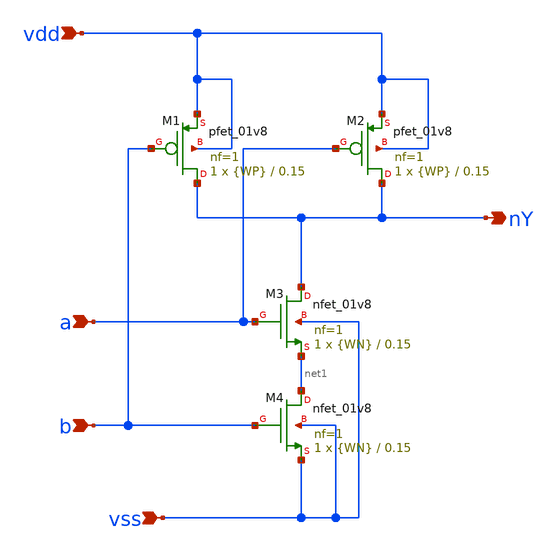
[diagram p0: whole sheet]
** sch_path: eamta2021/sch/nand/schNand.sch
**.subckt schNand vdd vss a b nY
*.ipin vdd
*.ipin vss
*.ipin a
*.ipin b
*.opin nY
XM1 nY b vdd vdd sky130_fd_pr__pfet_01v8 L=0.15 W={WP} nf=1 ad='int((nf+1)/2) * W/nf * 0.29' as='int((nf+2)/2) * W/nf * 0.29'
+ pd='2*int((nf+1)/2) * (W/nf + 0.29)' ps='2*int((nf+2)/2) * (W/nf + 0.29)' nrd='0.29 / W' nrs='0.29 / W'
+ sa=0 sb=0 sd=0 mult=1 m=1
XM2 nY a vdd vdd sky130_fd_pr__pfet_01v8 L=0.15 W={WP} nf=1 ad='int((nf+1)/2) * W/nf * 0.29' as='int((nf+2)/2) * W/nf * 0.29'
+ pd='2*int((nf+1)/2) * (W/nf + 0.29)' ps='2*int((nf+2)/2) * (W/nf + 0.29)' nrd='0.29 / W' nrs='0.29 / W'
+ sa=0 sb=0 sd=0 mult=1 m=1
XM3 nY a net1 vss sky130_fd_pr__nfet_01v8 L=0.15 W={WN} nf=1 ad='int((nf+1)/2) * W/nf * 0.29' as='int((nf+2)/2) * W/nf * 0.29'
+ pd='2*int((nf+1)/2) * (W/nf + 0.29)' ps='2*int((nf+2)/2) * (W/nf + 0.29)' nrd='0.29 / W' nrs='0.29 / W'
+ sa=0 sb=0 sd=0 mult=1 m=1
XM4 net1 b vss vss sky130_fd_pr__nfet_01v8 L=0.15 W={WN} nf=1 ad='int((nf+1)/2) * W/nf * 0.29' as='int((nf+2)/2) * W/nf * 0.29'
+ pd='2*int((nf+1)/2) * (W/nf + 0.29)' ps='2*int((nf+2)/2) * (W/nf + 0.29)' nrd='0.29 / W' nrs='0.29 / W'
+ sa=0 sb=0 sd=0 mult=1 m=1
**.ends
.end
